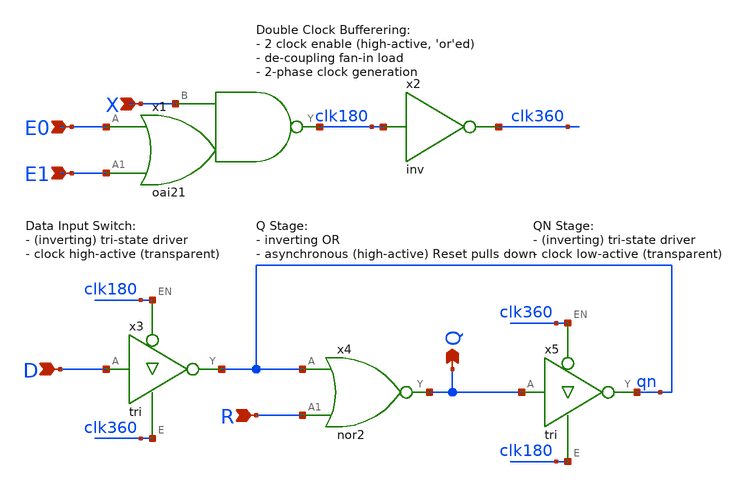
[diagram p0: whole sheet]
** sch_path: Sources/crafted/LATEERP.sch
**.subckt LATEERP X D Q E0 E1 R
*.ipin X
*.ipin D
*.opin Q
*.ipin E0
*.ipin E1
*.ipin R
x2 clk180 clk360 VDD GND inv Wmin=1.5u Lmin=1u g=2 m=1
x3 D clk180 clk360 qn VDD GND tri Wmin=1.5u Lmin=1u g=2 m=1
x5 Q clk360 clk180 qn VDD GND tri Wmin=1.5u Lmin=1u g=2 m=1
x4 Q qn R VDD GND nor2 Wmin=1.5u Lmin=1u g=2 m=1
x1 E0 E1 clk180 X VDD GND oai21 Wmin=1.5u Lmin=1u g=2 m=1
**.ends
.end
